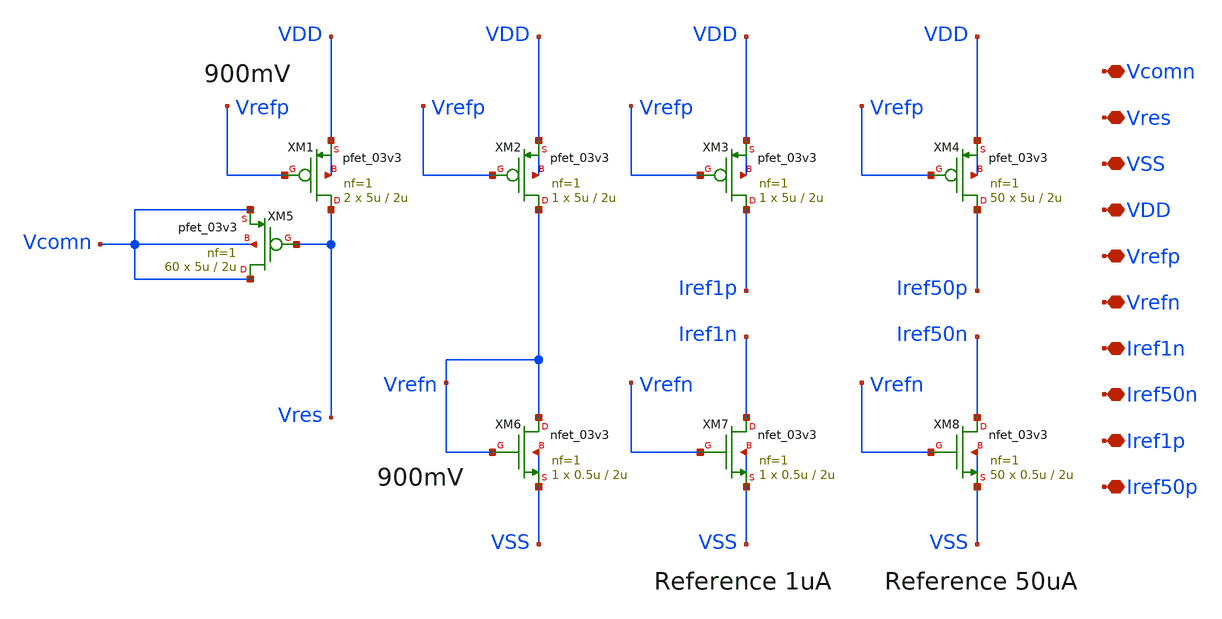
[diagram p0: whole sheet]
** sch_path: designs/current_reference_second_stage/xschem/current_reference_second_stage.sch
**.subckt current_reference_second_stage VDD VSS Vrefp Vrefn Iref1n Iref50n Iref1p Iref50p Vres
*+ Vcomn
*.iopin VDD
*.iopin VSS
*.iopin Vrefp
*.iopin Vrefn
*.iopin Iref1n
*.iopin Iref50n
*.iopin Iref1p
*.iopin Iref50p
*.iopin Vres
*.iopin Vcomn
XM6 Vrefn Vrefn VSS VSS nfet_03v3 L=2u W=0.5u nf=1 ad='int((nf+1)/2) * W/nf * 0.18u' as='int((nf+2)/2) * W/nf * 0.18u'
+ pd='2*int((nf+1)/2) * (W/nf + 0.18u)' ps='2*int((nf+2)/2) * (W/nf + 0.18u)' nrd='0.18u / W' nrs='0.18u / W'
+ sa=0 sb=0 sd=0 m=1
XM5 Vcomn Vres Vcomn Vcomn pfet_03v3 L=2u W=5u nf=1 ad='int((nf+1)/2) * W/nf * 0.18u' as='int((nf+2)/2) * W/nf * 0.18u'
+ pd='2*int((nf+1)/2) * (W/nf + 0.18u)' ps='2*int((nf+2)/2) * (W/nf + 0.18u)' nrd='0.18u / W' nrs='0.18u / W'
+ sa=0 sb=0 sd=0 m=60
XM1 Vres Vrefp VDD VDD pfet_03v3 L=2u W=5u nf=1 ad='int((nf+1)/2) * W/nf * 0.18u' as='int((nf+2)/2) * W/nf * 0.18u'
+ pd='2*int((nf+1)/2) * (W/nf + 0.18u)' ps='2*int((nf+2)/2) * (W/nf + 0.18u)' nrd='0.18u / W' nrs='0.18u / W'
+ sa=0 sb=0 sd=0 m=2
XM2 Vrefn Vrefp VDD VDD pfet_03v3 L=2u W=5u nf=1 ad='int((nf+1)/2) * W/nf * 0.18u' as='int((nf+2)/2) * W/nf * 0.18u'
+ pd='2*int((nf+1)/2) * (W/nf + 0.18u)' ps='2*int((nf+2)/2) * (W/nf + 0.18u)' nrd='0.18u / W' nrs='0.18u / W'
+ sa=0 sb=0 sd=0 m=1
XM3 Iref1p Vrefp VDD VDD pfet_03v3 L=2u W=5u nf=1 ad='int((nf+1)/2) * W/nf * 0.18u' as='int((nf+2)/2) * W/nf * 0.18u'
+ pd='2*int((nf+1)/2) * (W/nf + 0.18u)' ps='2*int((nf+2)/2) * (W/nf + 0.18u)' nrd='0.18u / W' nrs='0.18u / W'
+ sa=0 sb=0 sd=0 m=1
XM4 Iref50p Vrefp VDD VDD pfet_03v3 L=2u W=5u nf=1 ad='int((nf+1)/2) * W/nf * 0.18u' as='int((nf+2)/2) * W/nf * 0.18u'
+ pd='2*int((nf+1)/2) * (W/nf + 0.18u)' ps='2*int((nf+2)/2) * (W/nf + 0.18u)' nrd='0.18u / W' nrs='0.18u / W'
+ sa=0 sb=0 sd=0 m=50
XM7 Iref1n Vrefn VSS VSS nfet_03v3 L=2u W=0.5u nf=1 ad='int((nf+1)/2) * W/nf * 0.18u' as='int((nf+2)/2) * W/nf * 0.18u'
+ pd='2*int((nf+1)/2) * (W/nf + 0.18u)' ps='2*int((nf+2)/2) * (W/nf + 0.18u)' nrd='0.18u / W' nrs='0.18u / W'
+ sa=0 sb=0 sd=0 m=1
XM8 Iref50n Vrefn VSS VSS nfet_03v3 L=2u W=0.5u nf=1 ad='int((nf+1)/2) * W/nf * 0.18u' as='int((nf+2)/2) * W/nf * 0.18u'
+ pd='2*int((nf+1)/2) * (W/nf + 0.18u)' ps='2*int((nf+2)/2) * (W/nf + 0.18u)' nrd='0.18u / W' nrs='0.18u / W'
+ sa=0 sb=0 sd=0 m=50
**.ends
.end
